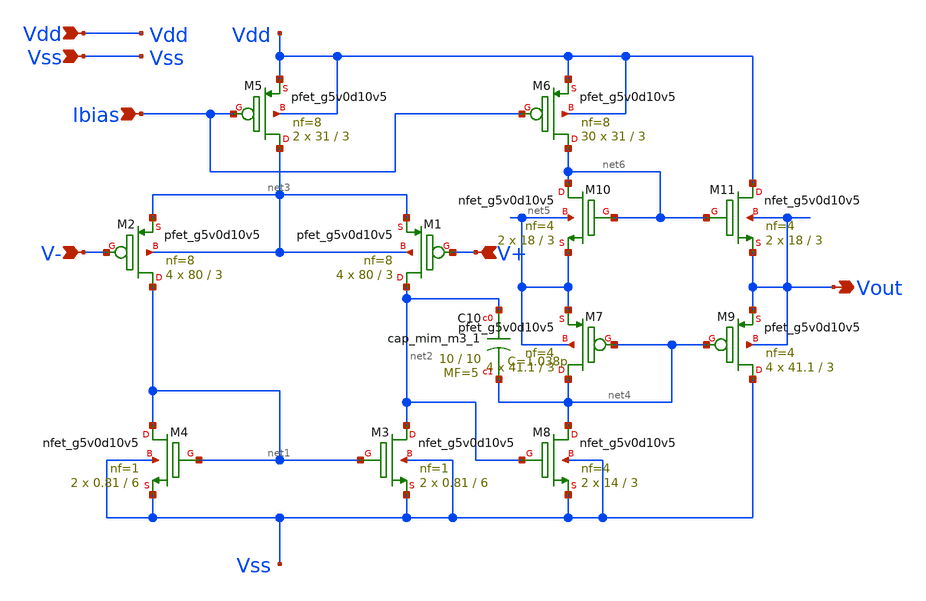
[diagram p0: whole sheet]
** sch_path: xschem/OP_AMP_PMOS_REVISE.sch
**.subckt OP_AMP_PMOS_REVISE V- V+ Vdd Vss Ibias Vout
*.ipin V-
*.ipin V+
*.ipin Vdd
*.ipin Vss
*.ipin Ibias
*.opin Vout
XM3 net2 net1 Vss Vss sky130_fd_pr__nfet_g5v0d10v5 L=6 W=0.81 nf=1 ad='int((1 + 1)/2) * 0.81 / 1 * 0.29'
+ as='int((1 + 2)/2) * 0.81 / 1 * 0.29' pd='2*int((1 + 1)/2) * (0.81 / 1 + 0.29)' ps='2*int((1 + 2)/2) * (0.81 / 1 + 0.29)'
+ nrd='0.29 / 0.81 ' nrs='0.29 / 0.81 ' sa=0 sb=0 sd=0 mult=2 m=2
XM1 net2 V+ net3 net3 sky130_fd_pr__pfet_g5v0d10v5 L=3 W=80 nf=8 ad='int((8 + 1)/2) * 80 / 8 * 0.29'
+ as='int((8 + 2)/2) * 80 / 8 * 0.29' pd='2*int((8 + 1)/2) * (80 / 8 + 0.29)' ps='2*int((8 + 2)/2) * (80 / 8 + 0.29)'
+ nrd='0.29 / 80 ' nrs='0.29 / 80 ' sa=0 sb=0 sd=0 mult=4 m=4
XM2 net1 V- net3 net3 sky130_fd_pr__pfet_g5v0d10v5 L=3 W=80 nf=8 ad='int((8 + 1)/2) * 80 / 8 * 0.29'
+ as='int((8 + 2)/2) * 80 / 8 * 0.29' pd='2*int((8 + 1)/2) * (80 / 8 + 0.29)' ps='2*int((8 + 2)/2) * (80 / 8 + 0.29)'
+ nrd='0.29 / 80 ' nrs='0.29 / 80 ' sa=0 sb=0 sd=0 mult=4 m=4
XM4 net1 net1 Vss Vss sky130_fd_pr__nfet_g5v0d10v5 L=6 W=0.81 nf=1 ad='int((1 + 1)/2) * 0.81 / 1 * 0.29'
+ as='int((1 + 2)/2) * 0.81 / 1 * 0.29' pd='2*int((1 + 1)/2) * (0.81 / 1 + 0.29)' ps='2*int((1 + 2)/2) * (0.81 / 1 + 0.29)'
+ nrd='0.29 / 0.81 ' nrs='0.29 / 0.81 ' sa=0 sb=0 sd=0 mult=2 m=2
XM8 net4 net2 Vss Vss sky130_fd_pr__nfet_g5v0d10v5 L=3 W=14 nf=4 ad='int((4 + 1)/2) * 14 / 4 * 0.29'
+ as='int((4 + 2)/2) * 14 / 4 * 0.29' pd='2*int((4 + 1)/2) * (14 / 4 + 0.29)' ps='2*int((4 + 2)/2) * (14 / 4 + 0.29)'
+ nrd='0.29 / 14 ' nrs='0.29 / 14 ' sa=0 sb=0 sd=0 mult=2 m=2
XM5 net3 Ibias Vdd Vdd sky130_fd_pr__pfet_g5v0d10v5 L=3 W=31 nf=8 ad='int((8 + 1)/2) * 31 / 8 * 0.29'
+ as='int((8 + 2)/2) * 31 / 8 * 0.29' pd='2*int((8 + 1)/2) * (31 / 8 + 0.29)' ps='2*int((8 + 2)/2) * (31 / 8 + 0.29)'
+ nrd='0.29 / 31 ' nrs='0.29 / 31 ' sa=0 sb=0 sd=0 mult=2 m=2
XM6 net6 Ibias Vdd Vdd sky130_fd_pr__pfet_g5v0d10v5 L=3 W=31 nf=8 ad='int((8 + 1)/2) * 31 / 8 * 0.29'
+ as='int((8 + 2)/2) * 31 / 8 * 0.29' pd='2*int((8 + 1)/2) * (31 / 8 + 0.29)' ps='2*int((8 + 2)/2) * (31 / 8 + 0.29)'
+ nrd='0.29 / 31 ' nrs='0.29 / 31 ' sa=0 sb=0 sd=0 mult=30 m=30
XM7 net4 net4 net5 net5 sky130_fd_pr__pfet_g5v0d10v5 L=3 W=41.1 nf=4 ad='int((4 + 1)/2) * 41.1 / 4 * 0.29'
+ as='int((4 + 2)/2) * 41.1 / 4 * 0.29' pd='2*int((4 + 1)/2) * (41.1 / 4 + 0.29)' ps='2*int((4 + 2)/2) * (41.1 / 4 + 0.29)'
+ nrd='0.29 / 41.1 ' nrs='0.29 / 41.1 ' sa=0 sb=0 sd=0 mult=4 m=4
XM9 Vss net4 Vout Vout sky130_fd_pr__pfet_g5v0d10v5 L=3 W=41.1 nf=4 ad='int((4 + 1)/2) * 41.1 / 4 * 0.29'
+ as='int((4 + 2)/2) * 41.1 / 4 * 0.29' pd='2*int((4 + 1)/2) * (41.1 / 4 + 0.29)' ps='2*int((4 + 2)/2) * (41.1 / 4 + 0.29)'
+ nrd='0.29 / 41.1 ' nrs='0.29 / 41.1 ' sa=0 sb=0 sd=0 mult=4 m=4
XM10 net6 net6 net5 net5 sky130_fd_pr__nfet_g5v0d10v5 L=3 W=18 nf=4 ad='int((4 + 1)/2) * 18 / 4 * 0.29'
+ as='int((4 + 2)/2) * 18 / 4 * 0.29' pd='2*int((4 + 1)/2) * (18 / 4 + 0.29)' ps='2*int((4 + 2)/2) * (18 / 4 + 0.29)'
+ nrd='0.29 / 18 ' nrs='0.29 / 18 ' sa=0 sb=0 sd=0 mult=2 m=2
XM11 Vdd net6 Vout Vout sky130_fd_pr__nfet_g5v0d10v5 L=3 W=18 nf=4 ad='int((4 + 1)/2) * 18 / 4 * 0.29'
+ as='int((4 + 2)/2) * 18 / 4 * 0.29' pd='2*int((4 + 1)/2) * (18 / 4 + 0.29)' ps='2*int((4 + 2)/2) * (18 / 4 + 0.29)'
+ nrd='0.29 / 18 ' nrs='0.29 / 18 ' sa=0 sb=0 sd=0 mult=2 m=2
XC10 net2 net4 sky130_fd_pr__cap_mim_m3_1 W=10 L=10 MF=5 m=5
**.ends
.end
